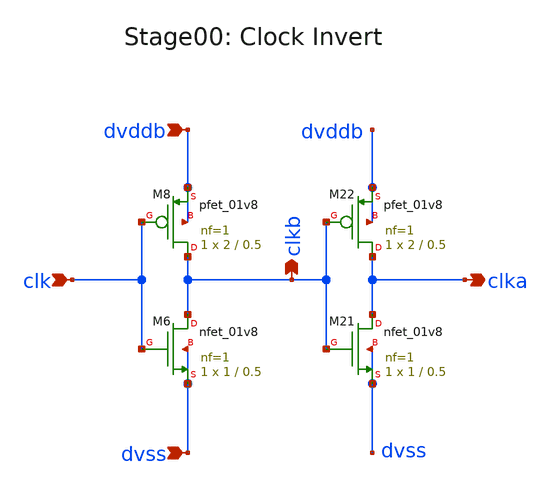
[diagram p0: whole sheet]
** sch_path: xschem/Stage0_clk_inv.sch
**.subckt Stage0_clk_inv dvss dvddb clka clk clkb
*.ipin dvss
*.ipin dvddb
*.opin clka
*.ipin clk
*.opin clkb
XM22 clka clkb dvddb dvddb sky130_fd_pr__pfet_01v8 L=0.5 W=2 nf=1 ad='int((nf+1)/2) * W/nf * 0.29' as='int((nf+2)/2) * W/nf * 0.29'
+ pd='2*int((nf+1)/2) * (W/nf + 0.29)' ps='2*int((nf+2)/2) * (W/nf + 0.29)' nrd='0.29 / W' nrs='0.29 / W'
+ sa=0 sb=0 sd=0 mult=1 m=1
XM8 clkb clk dvddb dvddb sky130_fd_pr__pfet_01v8 L=0.5 W=2 nf=1 ad='int((nf+1)/2) * W/nf * 0.29' as='int((nf+2)/2) * W/nf * 0.29'
+ pd='2*int((nf+1)/2) * (W/nf + 0.29)' ps='2*int((nf+2)/2) * (W/nf + 0.29)' nrd='0.29 / W' nrs='0.29 / W'
+ sa=0 sb=0 sd=0 mult=1 m=1
XM6 clkb clk dvss dvss sky130_fd_pr__nfet_01v8 L=0.5 W=1 nf=1 ad='int((nf+1)/2) * W/nf * 0.29' as='int((nf+2)/2) * W/nf * 0.29'
+ pd='2*int((nf+1)/2) * (W/nf + 0.29)' ps='2*int((nf+2)/2) * (W/nf + 0.29)' nrd='0.29 / W' nrs='0.29 / W'
+ sa=0 sb=0 sd=0 mult=1 m=1
XM21 clka clkb dvss dvss sky130_fd_pr__nfet_01v8 L=0.5 W=1 nf=1 ad='int((nf+1)/2) * W/nf * 0.29' as='int((nf+2)/2) * W/nf * 0.29'
+ pd='2*int((nf+1)/2) * (W/nf + 0.29)' ps='2*int((nf+2)/2) * (W/nf + 0.29)' nrd='0.29 / W' nrs='0.29 / W'
+ sa=0 sb=0 sd=0 mult=1 m=1
**.ends
.end
